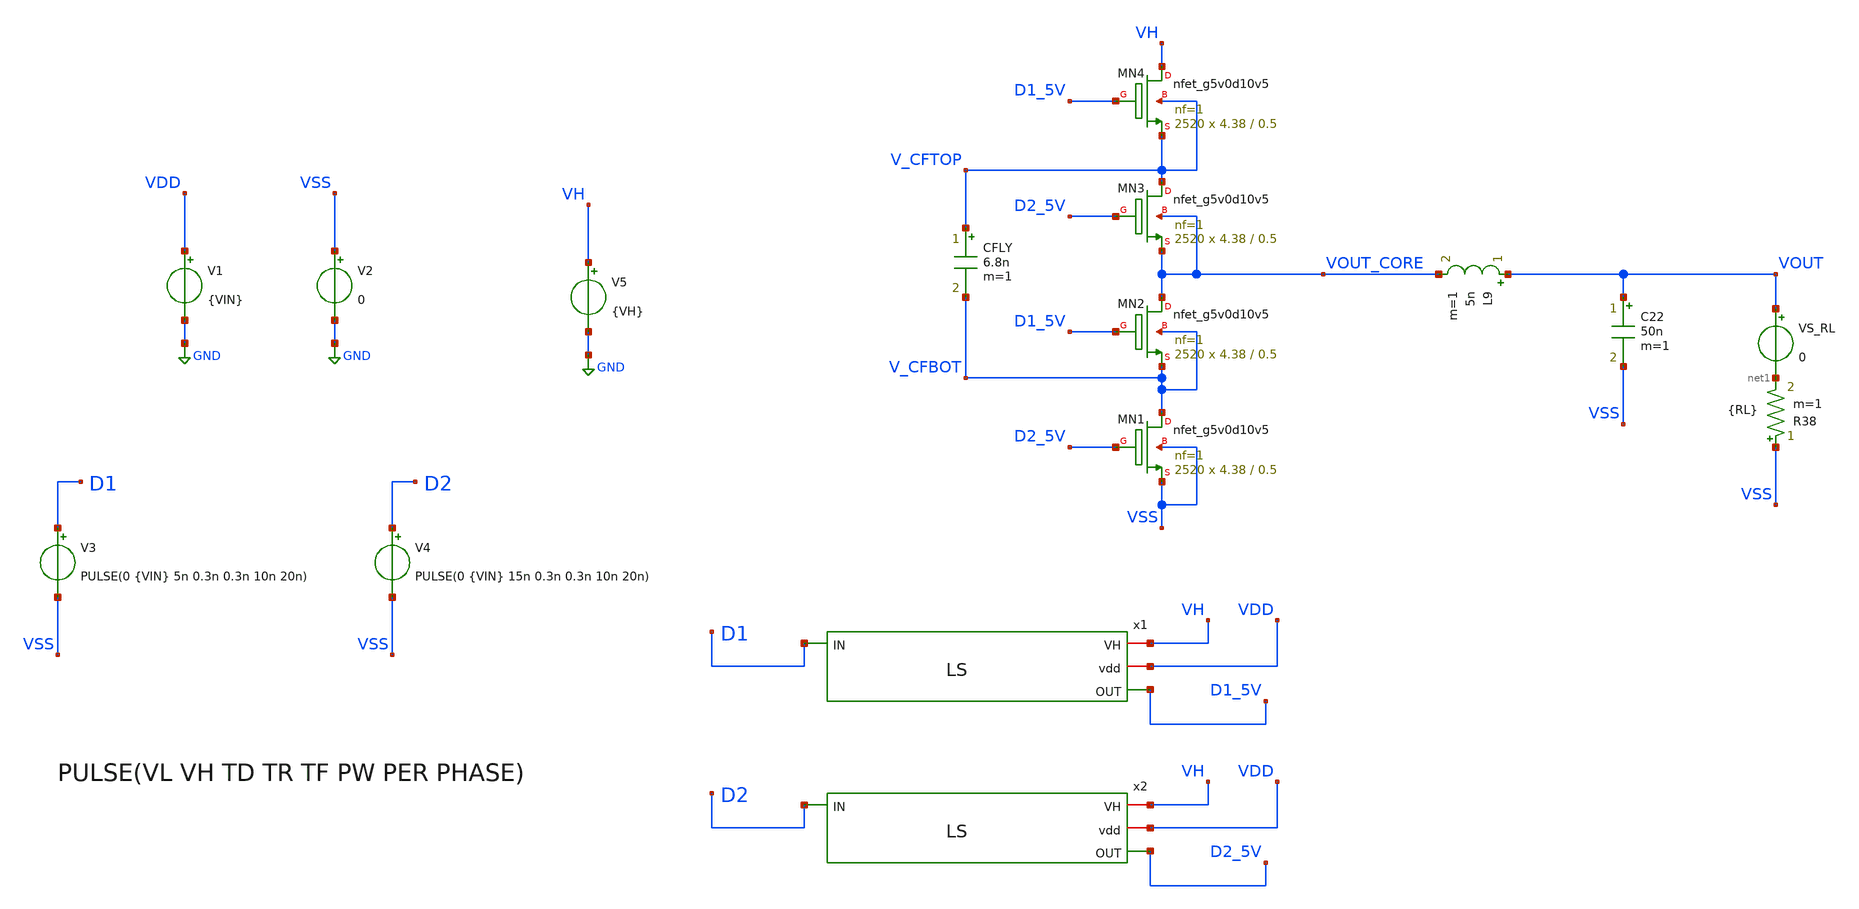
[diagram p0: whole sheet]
** sch_path: xschem/dev_switches/DCDC_v1p3_100MHz_NMOS.sch
**.subckt DCDC_v1p3_100MHz_NMOS
XMN2 VOUT_CORE D1_5V V_CFBOT V_CFBOT sky130_fd_pr__nfet_g5v0d10v5 L=0.5 W=4.38 nf=1 ad='int((nf+1)/2) * W/nf * 0.29'
+ as='int((nf+2)/2) * W/nf * 0.29' pd='2*int((nf+1)/2) * (W/nf + 0.29)' ps='2*int((nf+2)/2) * (W/nf + 0.29)'
+ nrd='0.29 / W' nrs='0.29 / W' sa=0 sb=0 sd=0 mult=2520 m=2520
XMN1 V_CFBOT D2_5V VSS VSS sky130_fd_pr__nfet_g5v0d10v5 L=0.5 W=4.38 nf=1 ad='int((nf+1)/2) * W/nf * 0.29'
+ as='int((nf+2)/2) * W/nf * 0.29' pd='2*int((nf+1)/2) * (W/nf + 0.29)' ps='2*int((nf+2)/2) * (W/nf + 0.29)'
+ nrd='0.29 / W' nrs='0.29 / W' sa=0 sb=0 sd=0 mult=2520 m=2520
CFLY V_CFTOP V_CFBOT 6.8n m=1
V1 VDD GND {VIN}
V3 D1 VSS PULSE(0 {VIN} 5n 0.3n 0.3n 10n 20n)
V2 VSS GND 0
V4 D2 VSS PULSE(0 {VIN} 15n 0.3n 0.3n 10n 20n)
L9 VOUT VOUT_CORE 5n m=1
C22 VOUT VSS 50n m=1
R38 VSS net1 {RL} m=1
VS_RL VOUT net1 0
XMN3 V_CFTOP D2_5V VOUT_CORE VOUT_CORE sky130_fd_pr__nfet_g5v0d10v5 L=0.5 W=4.38 nf=1 ad='int((nf+1)/2) * W/nf * 0.29'
+ as='int((nf+2)/2) * W/nf * 0.29' pd='2*int((nf+1)/2) * (W/nf + 0.29)' ps='2*int((nf+2)/2) * (W/nf + 0.29)'
+ nrd='0.29 / W' nrs='0.29 / W' sa=0 sb=0 sd=0 mult=2520 m=2520
XMN4 VH D1_5V V_CFTOP V_CFTOP sky130_fd_pr__nfet_g5v0d10v5 L=0.5 W=4.38 nf=1 ad='int((nf+1)/2) * W/nf * 0.29'
+ as='int((nf+2)/2) * W/nf * 0.29' pd='2*int((nf+1)/2) * (W/nf + 0.29)' ps='2*int((nf+2)/2) * (W/nf + 0.29)'
+ nrd='0.29 / W' nrs='0.29 / W' sa=0 sb=0 sd=0 mult=2520 m=2520
x1 VH VDD D1_5V D1 LS
V5 VH GND {VH}
x2 VH VDD D2_5V D2 LS
**** begin user architecture code


.param VIN = 1.8
.param VH = 5
.param RL = 500
*.option temp=70
.option scale=1e-6
.ic v(V_CFTOP) = VIN/2
.ic v(V_CFBOT) = 0
*.probe vd(MP2:G:S)

.param mc_mm_switch=0
*.lib /usr/share/pdk/sky130A/libs.tech/ngspice/sky130.lib.spice tt
.lib /foss/pdk/sky130A/libs.tech/ngspice/sky130.lib.spice TT
*.include /usr/share/pdk/sky130A/libs.ref/sky130_fd_sc_hvl/spice/sky130_fd_sc_hvl.spice
*.include /home/jorge/Documents/Postdoc/share/pdk/sky130A/libs.ref/sky130_fd_sc_hvl/spice/sky130_fd_sc_hvl.spice
.options savecurrents
.control
save all
tran 0.4n 2u
write DCDC_v1p3_100MHz.raw
.endc


**** end user architecture code
**.ends
.GLOBAL GND
.end
